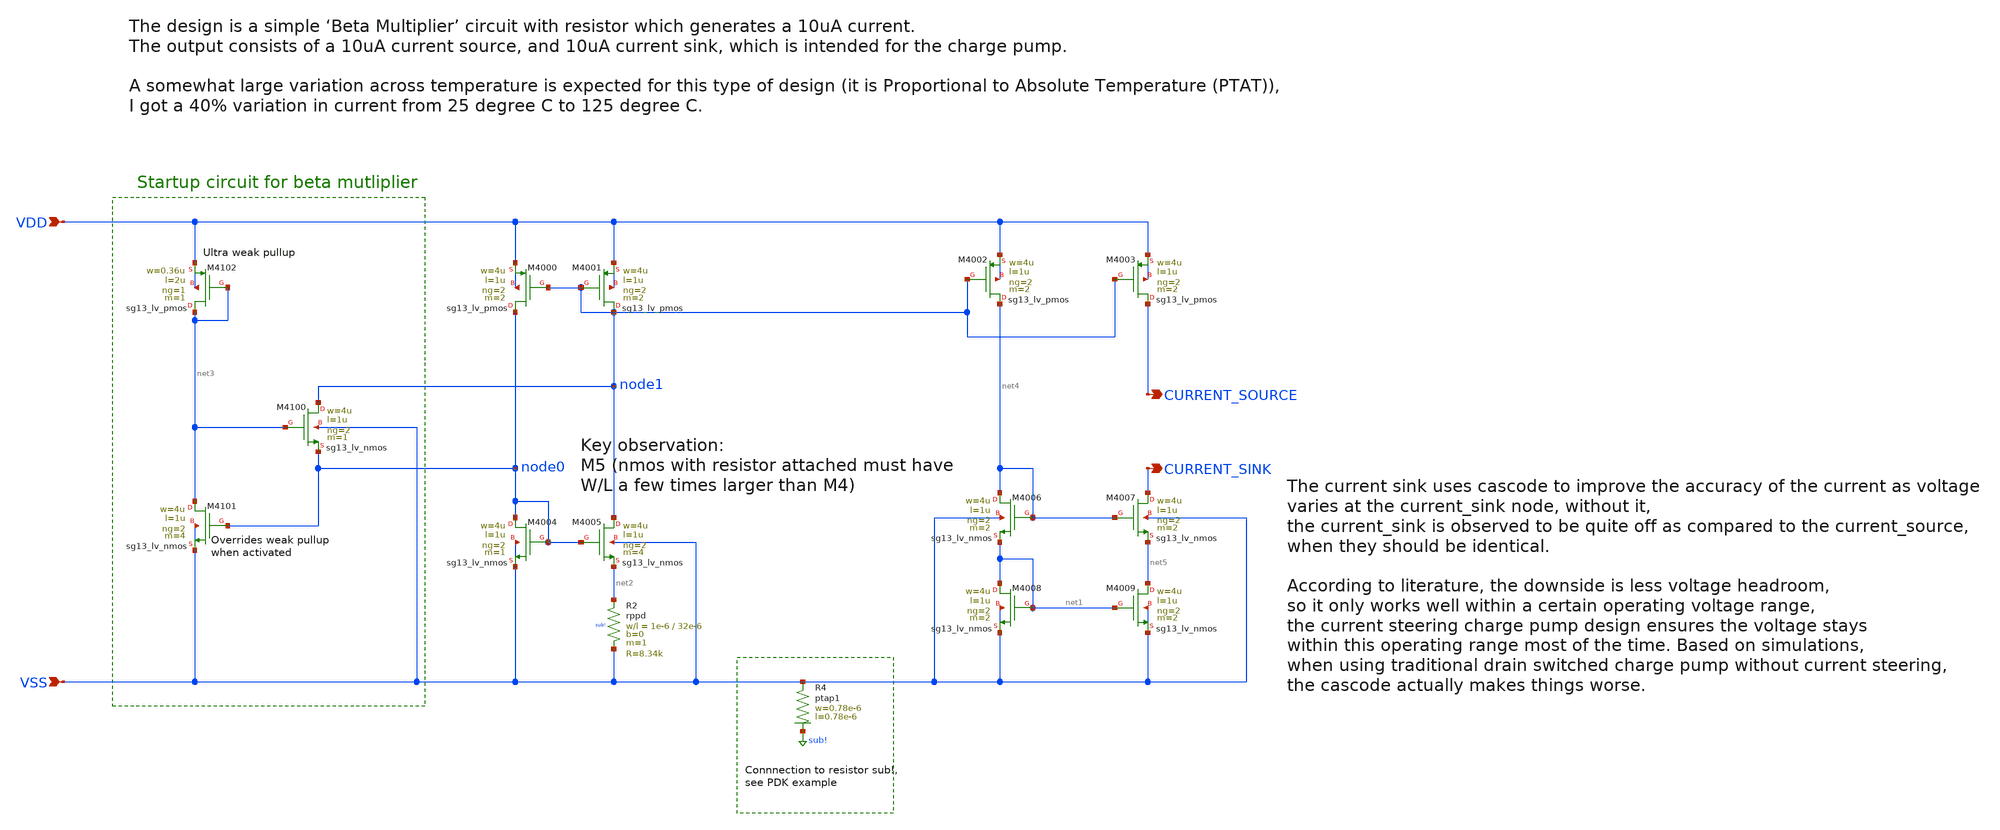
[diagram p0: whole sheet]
** sch_path: schematics/hx_charge_pump_current_generator.sch
**.subckt hx_charge_pump_current_generator VDD VSS CURRENT_SOURCE CURRENT_SINK
*.ipin VDD
*.ipin VSS
*.opin CURRENT_SOURCE
*.opin CURRENT_SINK
XM4002 net4 node1 VDD VDD sg13_lv_pmos w=4u l=1u ng=2 m=2 mm_ok=1
XM4009 net5 net1 VSS VSS sg13_lv_nmos w=4u l=1u ng=2 m=2 mm_ok=1
XM4008 net1 net1 VSS VSS sg13_lv_nmos w=4u l=1u ng=2 m=2 mm_ok=1
XM4003 CURRENT_SOURCE node1 VDD VDD sg13_lv_pmos w=4u l=1u ng=2 m=2 mm_ok=1
XM4000 node0 node1 VDD VDD sg13_lv_pmos w=4u l=1u ng=2 m=2 mm_ok=1
XM4001 node1 node1 VDD VDD sg13_lv_pmos w=4u l=1u ng=2 m=2 mm_ok=1
XM4004 node0 node0 VSS VSS sg13_lv_nmos w=4u l=1u ng=2 m=1 mm_ok=1
XM4005 node1 node0 net2 VSS sg13_lv_nmos w=4u l=1u ng=2 m=4 mm_ok=1
XR2 net2 VSS sub! rppd w=1e-6 l=32e-6 m=1 b=0 mm_ok=1
XM4102 net3 net3 VDD VDD sg13_lv_pmos w=0.36u l=2u ng=1 m=1 mm_ok=1
XM4100 node1 net3 node0 VSS sg13_lv_nmos w=4u l=1u ng=2 m=1 mm_ok=1
XM4101 net3 node0 VSS VSS sg13_lv_nmos w=4u l=1u ng=2 m=4 mm_ok=1
XR4 VSS sub! ptap1 R=262.8 w=0.78e-6 l=0.78e-6
XM4006 net4 net4 net1 VSS sg13_lv_nmos w=4u l=1u ng=2 m=2 mm_ok=1
XM4007 CURRENT_SINK net4 net5 VSS sg13_lv_nmos w=4u l=1u ng=2 m=2 mm_ok=1
**.ends
.GLOBAL sub!
.end
